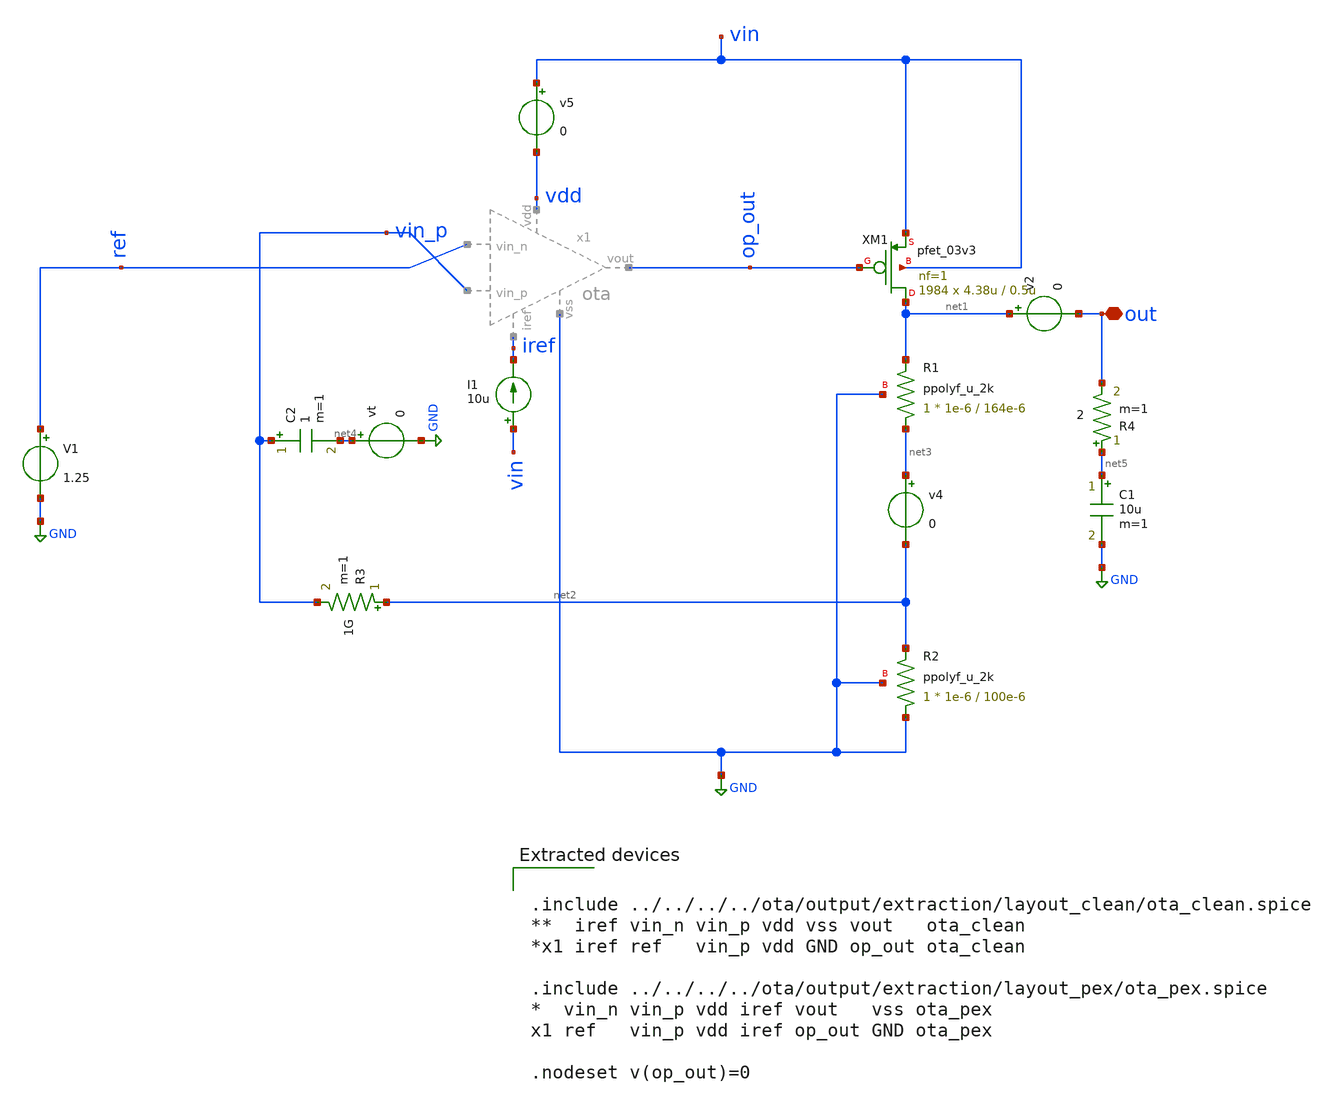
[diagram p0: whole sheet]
** sch_path: LDO/xschem/ldo/test/openloop.sch

.include $env(PDK_ROOT)/$env(PDK)/libs.tech/ngspice/design.ngspice
.lib $env(PDK_ROOT)/$env(PDK)/libs.tech/ngspice/sm141064.ngspice typical
.lib $env(PDK_ROOT)/$env(PDK)/libs.tech/ngspice/sm141064.ngspice res_typical

.lib $env(PDK_ROOT)/$env(PDK)/libs.tech/ngspice/sm141064.ngspice cap_mim
.lib $env(PDK_ROOT)/$env(PDK)/libs.tech/ngspice/sm141064.ngspice mimcap_typical

**.subckt openloop out
*.iopin out
I1 vin iref 10u
V1 ref GND 1.25
XM1 net1 op_out vin vin pfet_03v3 L=0.5u W=4.38u nf=1 ad='int((nf+1)/2) * W/nf * 0.18u' as='int((nf+2)/2) * W/nf * 0.18u'
+ pd='2*int((nf+1)/2) * (W/nf + 0.18u)' ps='2*int((nf+2)/2) * (W/nf + 0.18u)' nrd='0.18u / W' nrs='0.18u / W'
+ sa=0 sb=0 sd=0 m=1984
XR1 net3 net1 GND ppolyf_u_2k r_width=1e-6 r_length=164e-6 m=1
XR2 GND net2 GND ppolyf_u_2k r_width=1e-6 r_length=100e-6 m=1
v4 net3 net2 0
vt net4 GND 0
v2 net1 out 0
v5 vin vdd 0
R3 net2 vin_p 1G m=1
C2 vin_p net4 1 m=1
C1 net5 GND 10u m=1
R4 net5 out 2 m=1
**** begin user architecture code


.param R=66k
*.param R=33
R10 out 0 {R}
*IL out 0 PWL(0 0.1m 10u 0.1m 20u 10m 30u 10m)
*CL out 0 10u

.param iref = 10u
.param vdd  = 5
.param vss  = 0.0
.param vcm  = 1.25
.param vac  = 60m
.param w857 = 5u
.param l857 = 1u
.param m857 = 1
.param wpar = 10u
.param lpar = 1u
.param mpar = 1
.param w34  = 10u
.param l34  = 1u
.param m34  = 1
.param w6   = 100u
.param l6   = 1u
.param m6   = 1

.param m5   = 1
.param m7   = 5

Vs vin 0 5

.nodeset v(out)=0
.nodeset v(x1.pos)=0


*Stability_Analysis (openloop)
.control
reset
alter Vs AC=0
alter Vt AC =1
ac dec 100 1 1G
let phase_val = 180/PI*cph(out)
plot phase_val vdb(out)
meas ac pm FIND phase_val WHEN vdb(out)=0
meas ac cut_freq FIND frequency WHEN vdb(out)=0
*plot (180/pi)*vp(out)
*let gm0=@m.xm0.m0[gm]
*let Zout=(1.5)/(gm0*v(op_out))
*let Zout2=v(out)/gm0
*plot vdb(Zout2)
*wrdata /foss/designs/LDO_Design/data/data_PSRR.dat vdb(out)


op
print @m.x1.xm8.m0[vgs]-@m.x1.xm8.m0[vth]
print @m.x1.xm8.m0[vds]
print @m.x1.xm8.m0[id]
print **************
print @m.x1.xm7.m0[vgs]-@m.x1.xm7.m0[vth]
print @m.x1.xm7.m0[vds]
print @m.x1.xm7.m0[id]
print **************
print @m.x1.xm6.m0[vgs]-@m.x1.xm6.m0[vth]
print @m.x1.xm6.m0[vds]
print @m.x1.xm6.m0[gm]
print @m.x1.xm6.m0[gm]/@m.x1.xm6.m0[id]
print **************
print @m.x1.xm5.m0[vgs]-@m.x1.xm5.m0[vth]
print @m.x1.xm5.m0[vds]
print @m.x1.xm5.m0[id]
print **************
print @m.x1.xm1.m0[vgs]-@m.x1.xm1.m0[vth]
print @m.x1.xm1.m0[vds]
print @m.x1.xm1.m0[id]
print @m.x1.xm1.m0[gm]
print @m.x1.xm1.m0[gm]/@m.x1.xm1.m0[id]
print **************
print @m.x1.xm2.m0[vgs]-@m.x1.xm2.m0[vth]
print @m.x1.xm2.m0[vds]
print @m.x1.xm2.m0[id]
print @m.x1.xm2.m0[gm]
print @m.x1.xm2.m0[gm]/@m.x1.xm2.m0[id]
print **************
print @m.x1.xm3.m0[vgs]-@m.x1.xm3.m0[vth]
print @m.x1.xm3.m0[vds]
print @m.x1.xm3.m0[id]
print **************
print @m.x1.xm4.m0[vgs]-@m.x1.xm4.m0[vth]
print @m.x1.xm4.m0[vds]
print @m.x1.xm4.m0[id]

print v(op_out)
print v(out)

.endc






.include ../../../../ota/output/extraction/layout_clean/ota_clean.spice
**  iref vin_n vin_p vdd vss vout   ota_clean
*x1 iref ref   vin_p vdd GND op_out ota_clean

.include ../../../../ota/output/extraction/layout_pex/ota_pex.spice
*  vin_n vin_p vdd iref vout   vss ota_pex
x1 ref   vin_p vdd iref op_out GND ota_pex

.nodeset v(op_out)=0


**** end user architecture code
**.ends
.GLOBAL GND
.end
